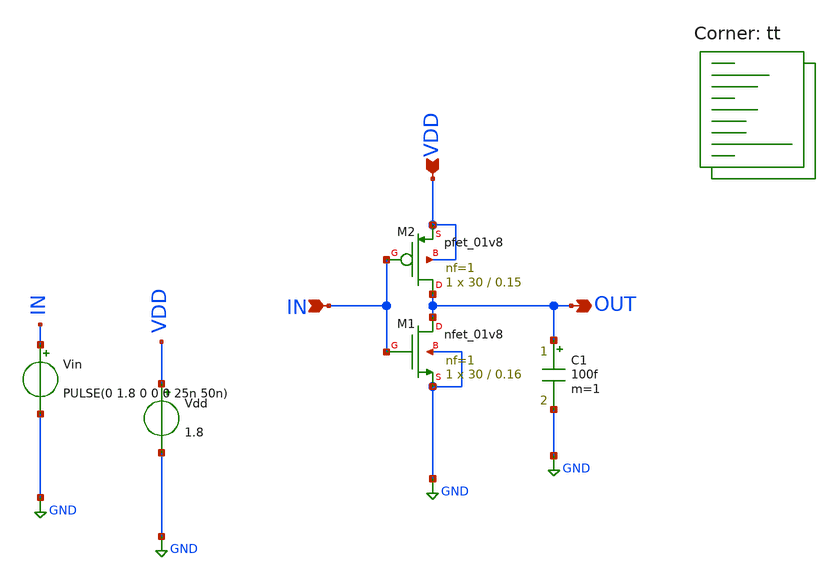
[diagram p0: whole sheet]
** sch_path: sizing-inverter.sch
**.subckt sizing-inverter IN VDD OUT
*.ipin IN
*.ipin VDD
*.opin OUT
Vin IN GND PULSE(0 1.8 0 0 0 25n 50n)
Vdd VDD GND 1.8
XM1 OUT IN GND GND sky130_fd_pr__nfet_01v8 L=0.16 W=30 nf=1 ad='int((nf+1)/2) * W/nf * 0.29' as='int((nf+2)/2) * W/nf * 0.29'
+ pd='2*int((nf+1)/2) * (W/nf + 0.29)' ps='2*int((nf+2)/2) * (W/nf + 0.29)' nrd='0.29 / W' nrs='0.29 / W'
+ sa=0 sb=0 sd=0 mult=1 m=1
XM2 OUT IN VDD VDD sky130_fd_pr__pfet_01v8 L=0.15 W=30 nf=1 ad='int((nf+1)/2) * W/nf * 0.29' as='int((nf+2)/2) * W/nf * 0.29'
+ pd='2*int((nf+1)/2) * (W/nf + 0.29)' ps='2*int((nf+2)/2) * (W/nf + 0.29)' nrd='0.29 / W' nrs='0.29 / W'
+ sa=0 sb=0 sd=0 mult=1 m=1
C1 OUT GND 100f m=1
**** begin user architecture code
.lib $::SKYWATER_MODELS/sky130.lib.spice tt


.options savecurrents

.control
save all

setplot const
let nmos_index = 0
let nmos_initial = 10
let nmos_w = nmos_initial
let nmos_final = 30
let nmos_step = 1

let nmos_length = ceil((nmos_final - nmos_initial)/nmos_step)

let pmos_index = 0
let pmos_initial = 10
let pmos_w = pmos_initial
let pmos_final = 30
let pmos_step = 5

while nmos_w < nmos_final

  alter @m.xm1.msky130_fd_pr__nfet_01v8[w] = nmos_w

  setplot const
  let switching_points = vector(nmos_length)
  let asymmetricity = vector(nmos_length)
  let width = vector(nmos_length)

  let minimum_asym = 100
  let minimum_width_pmos = 100

**** Find least asymmetric pmos_w ****
  while pmos_w < pmos_final

    alter @m.xm2.msky130_fd_pr__pfet_01v8[w] = pmos_w

    tran 10p 50n ; Run transient analysis using a symmetric pulse of period 25n

    meas tran rise_time TRIG v(out) VAL=0.1 RISE=1 TARG v(out) VAL=1.62 RISE=1
    meas tran fall_time TRIG v(out) VAL=1.62 FALL=1 TARG v(out) VAL=0.1 FALL=1

    let diff = abs( $&rise_time - $&fall_time ) ; Create array of diffs

    if diff < minimum_asym
      let minimum_asym = diff
      let minimum_width_pmos = pmos_w
    end
    let pmos_w = pmos_w + pmos_step
  end

  alter @m.xm2.msky130_fd_pr__pfet_01v8[W] = minimum_width_pmos

**** Find switching point for aforementioned pmos_w ****

  dc vin 0 1.8 1m ; Run dc analysis, check for operating point

  meas dc switching_point WHEN v(out)=v(in) CROSS=LAST

  let switching_points[nmos_index] = $&switching_point
  let width[nmos_index] = minimum_width_pmos
  print nmos_index minimum_width_pmos

  let nmos_w = nmos_w + nmos_step
  let nmos_index = nmos_index + 1
end

plot switching_points vs width

.endc


**** end user architecture code
**.ends
.GLOBAL GND
.end
